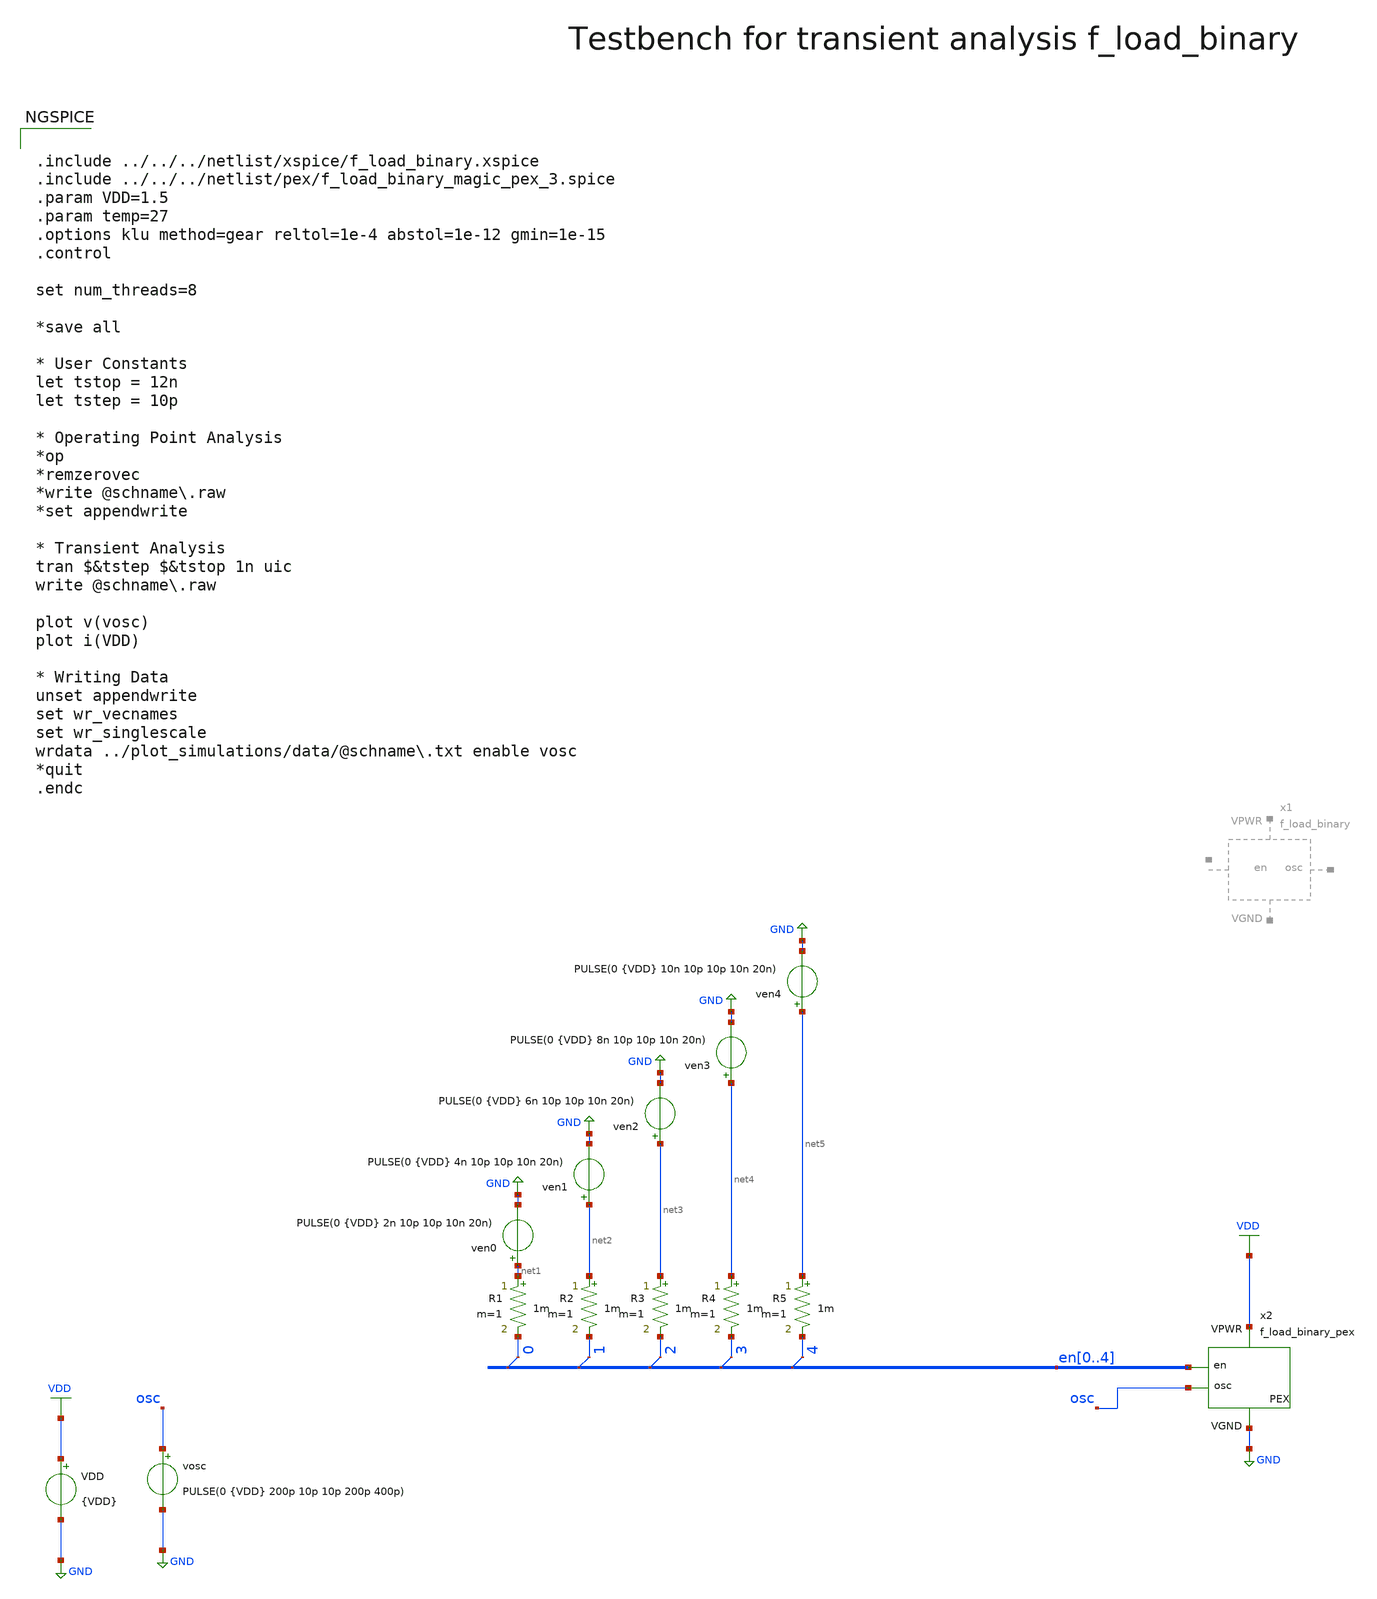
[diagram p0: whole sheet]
** sch_path: macros/heichips26_digital_project/macros/f_load_binary/testbenches/xschem/f_load_binary_tb_tran.sch
**.subckt f_load_binary_tb_tran
VDD VDD GND {VDD}
ven0 net1 GND PULSE(0 {VDD} 2n 10p 10p 10n 20n)
x2 VDD GND en0 en1 en2 en3 en4 osc f_load_binary_pex
* tap: en[0..4] --> en0
* tap: en[0..4] --> en2
* tap: en[0..4] --> en4
* tap: en[0..4] --> en3
* tap: en[0..4] --> en1
vosc osc GND PULSE(0 {VDD} 200p 10p 10p 200p 400p)
R1 net1 en0 1m m=1
R2 net2 en1 1m m=1
R3 net3 en2 1m m=1
R4 net4 en3 1m m=1
R5 net5 en4 1m m=1
ven1 net2 GND PULSE(0 {VDD} 4n 10p 10p 10n 20n)
ven2 net3 GND PULSE(0 {VDD} 6n 10p 10p 10n 20n)
ven3 net4 GND PULSE(0 {VDD} 8n 10p 10p 10n 20n)
ven4 net5 GND PULSE(0 {VDD} 10n 10p 10p 10n 20n)
**** begin user architecture code


.include ../../../netlist/xspice/f_load_binary.xspice
.include ../../../netlist/pex/f_load_binary_magic_pex_3.spice
.param VDD=1.5
.param temp=27
.options klu method=gear reltol=1e-4 abstol=1e-12 gmin=1e-15
.control

set num_threads=8

*save all

* User Constants
let tstop = 12n
let tstep = 10p

* Operating Point Analysis
*op
*remzerovec
*write @schname\.raw
*set appendwrite

* Transient Analysis
tran $&tstep $&tstop 1n uic
write @schname\.raw

plot v(vosc)
plot i(VDD)

* Writing Data
unset appendwrite
set wr_vecnames
set wr_singlescale
wrdata ../plot_simulations/data/@schname\.txt enable vosc
*quit
.endc


.lib cornerMOSlv.lib mos_tt
.lib cornerMOShv.lib mos_tt
.lib cornerRES.lib res_typ
.lib cornerDIO.lib dio_tt

**** end user architecture code
**.ends
.GLOBAL GND
.GLOBAL VDD
.end
